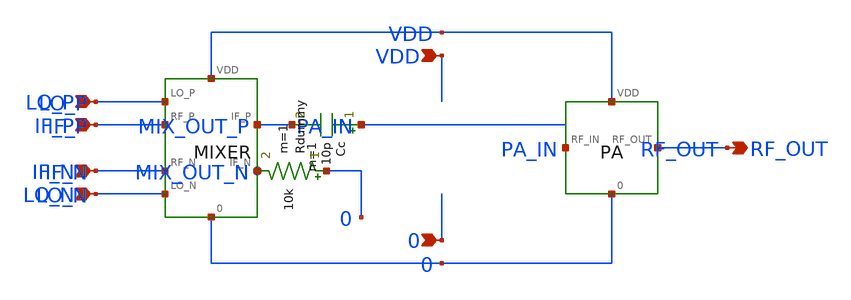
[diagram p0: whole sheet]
** sch_path: modules/PandaChip/designs/rf_trans/tx_top.sch
**.subckt tx_top IF_P IF_N LO_P LO_N RF_OUT VDD 0
*.ipin IF_P
*.ipin IF_N
*.ipin LO_P
*.ipin LO_N
*.opin RF_OUT
*.ipin VDD
*.ipin 0
X1 VDD 0 IF_P IF_N LO_P LO_N MIX_OUT_P MIX_OUT_N mixer
X2 VDD 0 PA_IN RF_OUT pa
Cc PA_IN MIX_OUT_P 10p m=1
Rdummy 0 MIX_OUT_N 10k m=1
**.ends

* expanding   symbol:  mixer.sym # of pins=8
** sym_path: modules/PandaChip/designs/rf_trans/mixer.sym
** sch_path: modules/PandaChip/designs/rf_trans/mixer.sch
.subckt mixer VDD 0 RF_P RF_N LO_P LO_N IF_P IF_N
*.ipin VDD
*.ipin 0
*.ipin RF_P
*.ipin RF_N
*.ipin LO_P
*.ipin LO_N
*.opin IF_P
*.opin IF_N
XM1 M1D RF_P TAIL 0 nfet_03v3 L=0.28u W=50u nf=5 ad='int((nf+1)/2) * W/nf * 0.18u' as='int((nf+2)/2) * W/nf * 0.18u'
+ pd='2*int((nf+1)/2) * (W/nf + 0.18u)' ps='2*int((nf+2)/2) * (W/nf + 0.18u)' nrd='0.18u / W' nrs='0.18u / W'
+ sa=0 sb=0 sd=0 m=1
XM2 M2D RF_N TAIL 0 nfet_03v3 L=0.28u W=50u nf=5 ad='int((nf+1)/2) * W/nf * 0.18u' as='int((nf+2)/2) * W/nf * 0.18u'
+ pd='2*int((nf+1)/2) * (W/nf + 0.18u)' ps='2*int((nf+2)/2) * (W/nf + 0.18u)' nrd='0.18u / W' nrs='0.18u / W'
+ sa=0 sb=0 sd=0 m=1
XM3 IF_P LO_P M1D 0 nfet_03v3 L=0.28u W=50u nf=5 ad='int((nf+1)/2) * W/nf * 0.18u' as='int((nf+2)/2) * W/nf * 0.18u'
+ pd='2*int((nf+1)/2) * (W/nf + 0.18u)' ps='2*int((nf+2)/2) * (W/nf + 0.18u)' nrd='0.18u / W' nrs='0.18u / W'
+ sa=0 sb=0 sd=0 m=1
XM4 IF_N LO_N M1D 0 nfet_03v3 L=0.28u W=50u nf=5 ad='int((nf+1)/2) * W/nf * 0.18u' as='int((nf+2)/2) * W/nf * 0.18u'
+ pd='2*int((nf+1)/2) * (W/nf + 0.18u)' ps='2*int((nf+2)/2) * (W/nf + 0.18u)' nrd='0.18u / W' nrs='0.18u / W'
+ sa=0 sb=0 sd=0 m=1
XM5 IF_P LO_N M2D 0 nfet_03v3 L=0.28u W=50u nf=5 ad='int((nf+1)/2) * W/nf * 0.18u' as='int((nf+2)/2) * W/nf * 0.18u'
+ pd='2*int((nf+1)/2) * (W/nf + 0.18u)' ps='2*int((nf+2)/2) * (W/nf + 0.18u)' nrd='0.18u / W' nrs='0.18u / W'
+ sa=0 sb=0 sd=0 m=1
XM6 IF_N LO_P M2D 0 nfet_03v3 L=0.28u W=50u nf=5 ad='int((nf+1)/2) * W/nf * 0.18u' as='int((nf+2)/2) * W/nf * 0.18u'
+ pd='2*int((nf+1)/2) * (W/nf + 0.18u)' ps='2*int((nf+2)/2) * (W/nf + 0.18u)' nrd='0.18u / W' nrs='0.18u / W'
+ sa=0 sb=0 sd=0 m=1
R1 VDD IF_P 2k m=1
R2 VDD IF_N 2k m=1
I1 TAIL 0 2m
.ends


* expanding   symbol:  pa.sym # of pins=4
** sym_path: modules/PandaChip/designs/rf_trans/pa.sym
** sch_path: modules/PandaChip/designs/rf_trans/pa.sch
.subckt pa VDD 0 RF_IN RF_OUT
*.ipin VDD
*.ipin RF_IN
*.opin RF_OUT
*.ipin 0
XM1 PA_D VBIAS 0 0 nfet_03v3 L=0.28u W=400u nf=40 ad='int((nf+1)/2) * W/nf * 0.18u' as='int((nf+2)/2) * W/nf * 0.18u'
+ pd='2*int((nf+1)/2) * (W/nf + 0.18u)' ps='2*int((nf+2)/2) * (W/nf + 0.18u)' nrd='0.18u / W' nrs='0.18u / W'
+ sa=0 sb=0 sd=0 m=1
L1 VDD PA_D 1u m=1
Cout RF_OUT PA_D 1n m=1
Cin VBIAS RF_IN 100p m=1
R1 VDD VBIAS 10k m=1
R2 VBIAS 0 10k m=1
.ends

.end
